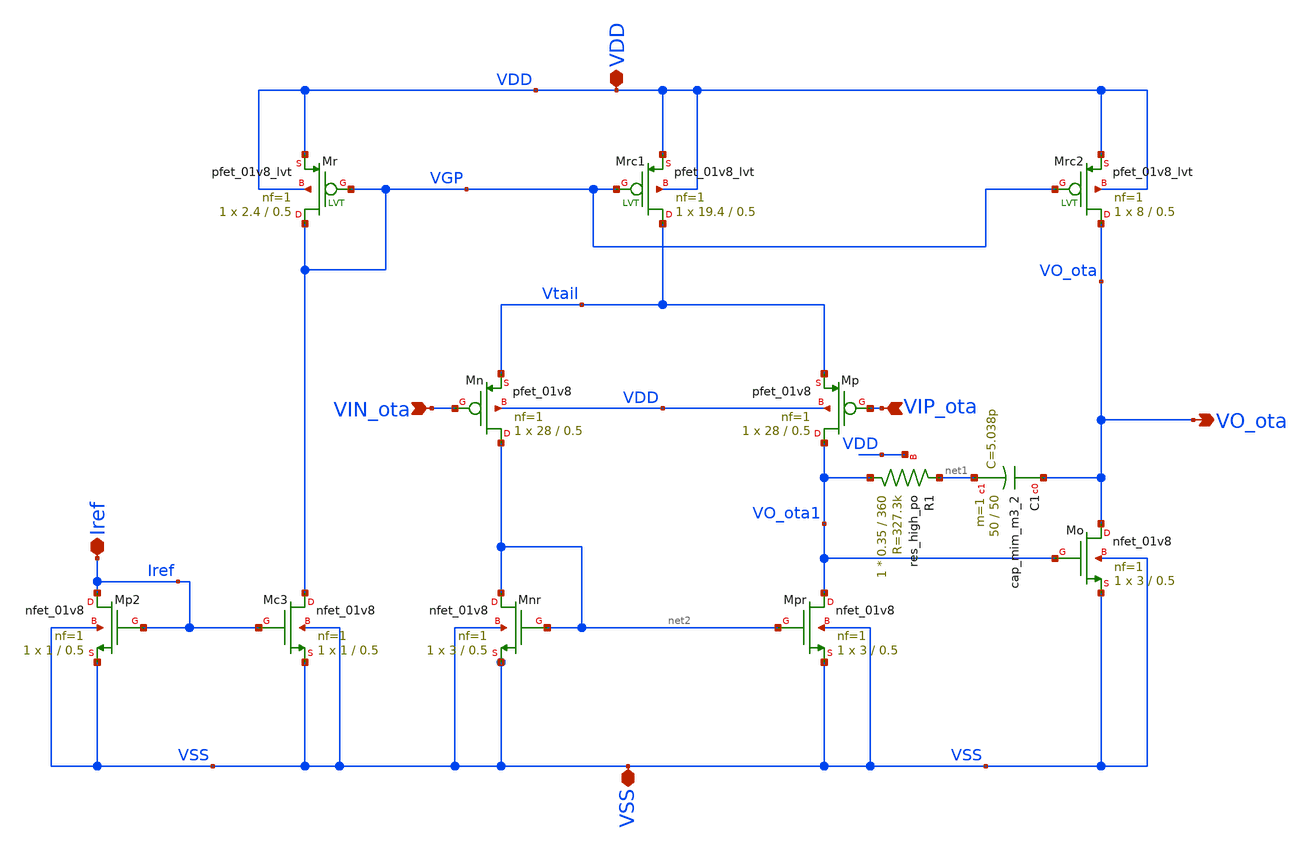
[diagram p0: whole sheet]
** sch_path: xschem/OTA.sch
**.subckt OTA VIN_ota VO_ota Iref VSS VDD VIP_ota
*.ipin VIN_ota
*.opin VO_ota
*.iopin Iref
*.iopin VSS
*.iopin VDD
*.ipin VIP_ota
XR1 VO_ota1 net1 VDD sky130_fd_pr__res_high_po W=0.35 L=360 mult=1 m=1
XC1 VO_ota net1 sky130_fd_pr__cap_mim_m3_2 W=50 L=50 MF=1 m=1
XMpr VO_ota1 net2 VSS VSS sky130_fd_pr__nfet_01v8 L=0.5 W=3 nf=1 ad='int((1 + 1)/2) * 3 / 1 * 0.29' as='int((1 + 2)/2) * 3 / 1 * 0.29'
+ pd='2*int((1 + 1)/2) * (3 / 1 + 0.29)' ps='2*int((1 + 2)/2) * (3 / 1 + 0.29)' nrd='0.29 / 3 ' nrs='0.29 / 3 '
+ sa=0 sb=0 sd=0 mult=1 m=1
XMnr net2 net2 VSS VSS sky130_fd_pr__nfet_01v8 L=0.5 W=3 nf=1 ad='int((1 + 1)/2) * 3 / 1 * 0.29' as='int((1 + 2)/2) * 3 / 1 * 0.29'
+ pd='2*int((1 + 1)/2) * (3 / 1 + 0.29)' ps='2*int((1 + 2)/2) * (3 / 1 + 0.29)' nrd='0.29 / 3 ' nrs='0.29 / 3 '
+ sa=0 sb=0 sd=0 mult=1 m=1
XMn net2 VIN_ota Vtail VDD sky130_fd_pr__pfet_01v8 L=0.5 W=28 nf=1 ad='int((1 + 1)/2) * 28 / 1 * 0.29'
+ as='int((1 + 2)/2) * 28 / 1 * 0.29' pd='2*int((1 + 1)/2) * (28 / 1 + 0.29)' ps='2*int((1 + 2)/2) * (28 / 1 + 0.29)'
+ nrd='0.29 / 28 ' nrs='0.29 / 28 ' sa=0 sb=0 sd=0 mult=1 m=1
XMp VO_ota1 VIP_ota Vtail VDD sky130_fd_pr__pfet_01v8 L=0.5 W=28 nf=1 ad='int((1 + 1)/2) * 28 / 1 * 0.29'
+ as='int((1 + 2)/2) * 28 / 1 * 0.29' pd='2*int((1 + 1)/2) * (28 / 1 + 0.29)' ps='2*int((1 + 2)/2) * (28 / 1 + 0.29)'
+ nrd='0.29 / 28 ' nrs='0.29 / 28 ' sa=0 sb=0 sd=0 mult=1 m=1
XMo VO_ota VO_ota1 VSS VSS sky130_fd_pr__nfet_01v8 L=0.5 W=3 nf=1 ad='int((1 + 1)/2) * 3 / 1 * 0.29'
+ as='int((1 + 2)/2) * 3 / 1 * 0.29' pd='2*int((1 + 1)/2) * (3 / 1 + 0.29)' ps='2*int((1 + 2)/2) * (3 / 1 + 0.29)'
+ nrd='0.29 / 3 ' nrs='0.29 / 3 ' sa=0 sb=0 sd=0 mult=1 m=1
XMc3 VGP Iref VSS VSS sky130_fd_pr__nfet_01v8 L=0.5 W=1 nf=1 ad='int((1 + 1)/2) * 1 / 1 * 0.29' as='int((1 + 2)/2) * 1 / 1 * 0.29'
+ pd='2*int((1 + 1)/2) * (1 / 1 + 0.29)' ps='2*int((1 + 2)/2) * (1 / 1 + 0.29)' nrd='0.29 / 1 ' nrs='0.29 / 1 '
+ sa=0 sb=0 sd=0 mult=1 m=1
XMp2 Iref Iref VSS VSS sky130_fd_pr__nfet_01v8 L=0.5 W=1 nf=1 ad='int((1 + 1)/2) * 1 / 1 * 0.29' as='int((1 + 2)/2) * 1 / 1 * 0.29'
+ pd='2*int((1 + 1)/2) * (1 / 1 + 0.29)' ps='2*int((1 + 2)/2) * (1 / 1 + 0.29)' nrd='0.29 / 1 ' nrs='0.29 / 1 '
+ sa=0 sb=0 sd=0 mult=1 m=1
XMr VGP VGP VDD VDD sky130_fd_pr__pfet_01v8_lvt L=0.5 W=2.4 nf=1 ad='int((1 + 1)/2) * 2.4 / 1 * 0.29'
+ as='int((1 + 2)/2) * 2.4 / 1 * 0.29' pd='2*int((1 + 1)/2) * (2.4 / 1 + 0.29)' ps='2*int((1 + 2)/2) * (2.4 / 1 + 0.29)'
+ nrd='0.29 / 2.4 ' nrs='0.29 / 2.4 ' sa=0 sb=0 sd=0 mult=1 m=1
XMrc1 Vtail VGP VDD VDD sky130_fd_pr__pfet_01v8_lvt L=0.5 W=19.4 nf=1 ad='int((1 + 1)/2) * 19.4 / 1 * 0.29'
+ as='int((1 + 2)/2) * 19.4 / 1 * 0.29' pd='2*int((1 + 1)/2) * (19.4 / 1 + 0.29)' ps='2*int((1 + 2)/2) * (19.4 / 1 + 0.29)'
+ nrd='0.29 / 19.4 ' nrs='0.29 / 19.4 ' sa=0 sb=0 sd=0 mult=1 m=1
XMrc2 VO_ota VGP VDD VDD sky130_fd_pr__pfet_01v8_lvt L=0.5 W=8 nf=1 ad='int((1 + 1)/2) * 8 / 1 * 0.29'
+ as='int((1 + 2)/2) * 8 / 1 * 0.29' pd='2*int((1 + 1)/2) * (8 / 1 + 0.29)' ps='2*int((1 + 2)/2) * (8 / 1 + 0.29)'
+ nrd='0.29 / 8 ' nrs='0.29 / 8 ' sa=0 sb=0 sd=0 mult=1 m=1
**.ends
.end
